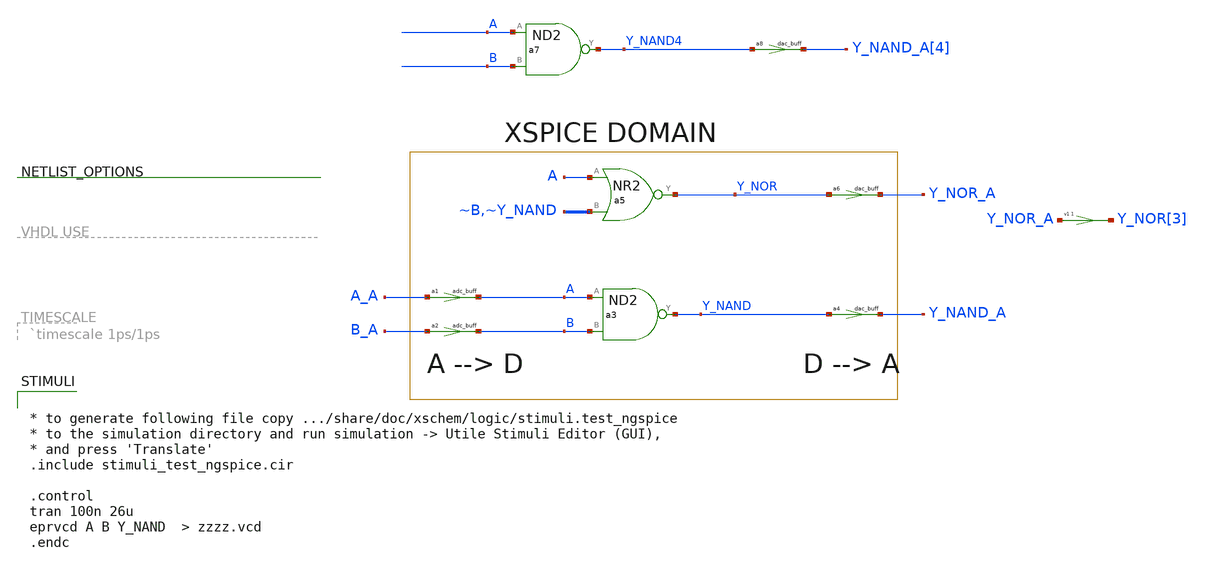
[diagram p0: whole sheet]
** sch_path: xschem_library/logic/test_ngspice.sch
**.subckt test_ngspice
a1 [ A_A ] [ A ] adc_buff
a2 [ B_A ] [ B ] adc_buff
a3 [ A B ] Y_NAND nand
a4 [ Y_NAND ] [ Y_NAND_A ] dac_buff
a6 [ Y_NOR ] [ Y_NOR_A ] dac_buff
a5 Y_NOR A ~B nr2
a7 [ A B ] Y_NAND4 nand
a8 [ Y_NAND4 ] [ Y_NAND_A[4] ] dac_buff
v1 Y_NOR[3] Y_NOR_A 0
**** begin user architecture code
.model adc_buff adc_bridge(in_low = 0.3 in_high = 0.7)


.model nand d_nand(rise_delay = 0.5e-9 fall_delay = 0.3e-9  input_load = 5e-15)

.model nor d_nor(rise_delay = 0.7e-9 fall_delay = 0.2e-9  input_load = 5e-15)

.model dac_buff  dac_bridge(out_low = 0 out_high = 1.2 out_undef = 0.6  input_load = 5.0e-15 t_rise
+ = 0.5e-9  t_fall = 0.2e-9)

**** end user architecture code
**.ends

* expanding   symbol:  nd2.sym # of pins=3
** sym_path: xschem_library/logic/nd2.sym
** sch_path: xschem_library/logic/nd2.sch
.subckt nd2 A B Y  delay=120 ps del=120
.ends


* expanding   symbol:  nr2.sym # of pins=3
** sym_path: xschem_library/logic/nr2.sym
** sch_path: xschem_library/logic/nr2.sch
.subckt nr2 Y A B  delay=200 ps del=200
*.opin Y
*.ipin A
*.ipin B
.ends

**** begin user architecture code


* to generate following file copy .../share/doc/xschem/logic/stimuli.test_ngspice
* to the simulation directory and run simulation -> Utile Stimuli Editor (GUI),
* and press 'Translate'
.include stimuli_test_ngspice.cir

.control
tran 100n 26u
eprvcd A B Y_NAND  > zzzz.vcd
.endc


**** end user architecture code
.end
